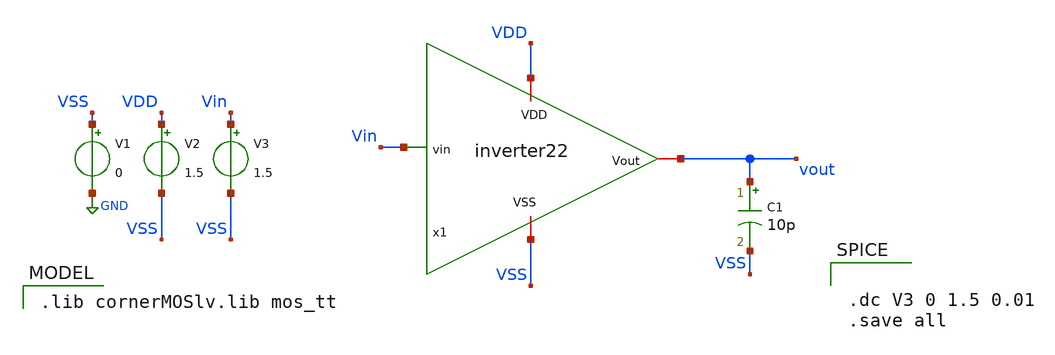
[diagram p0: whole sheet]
** sch_path: Lab2/inverter22_tb.sch
**.subckt inverter22_tb
V1 VSS GND 0
V2 VDD VSS 1.5
V3 Vin VSS 1.5
C1 vout VSS 10p m=1
x1 VDD Vin vout VSS inverter22
**** begin user architecture code
 .lib cornerMOSlv.lib mos_tt



.dc V3 0 1.5 0.01
.save all


**** end user architecture code
**.ends

* expanding   symbol:
*+  /home/fcastellanos/Documents/SEED_Bootcamp_ihp/Modulo_Analogico/Lab2/inverter22.sym # of pins=4
** sym_path: Lab2/inverter22.sym
** sch_path: Lab2/inverter22.sch
.subckt inverter22 VDD vin Vout VSS
*.ipin vin
*.iopin Vout
*.iopin VDD
*.iopin VSS
XM1 Vout vin VSS VSS sg13_lv_nmos w=1u l=1u ng=1 m=1 mm_ok=1
XM2 Vout vin VDD VDD sg13_lv_pmos w=3u l=1u ng=1 m=1 rfmode=1 mm_ok=1
.ends

.GLOBAL GND
.end
